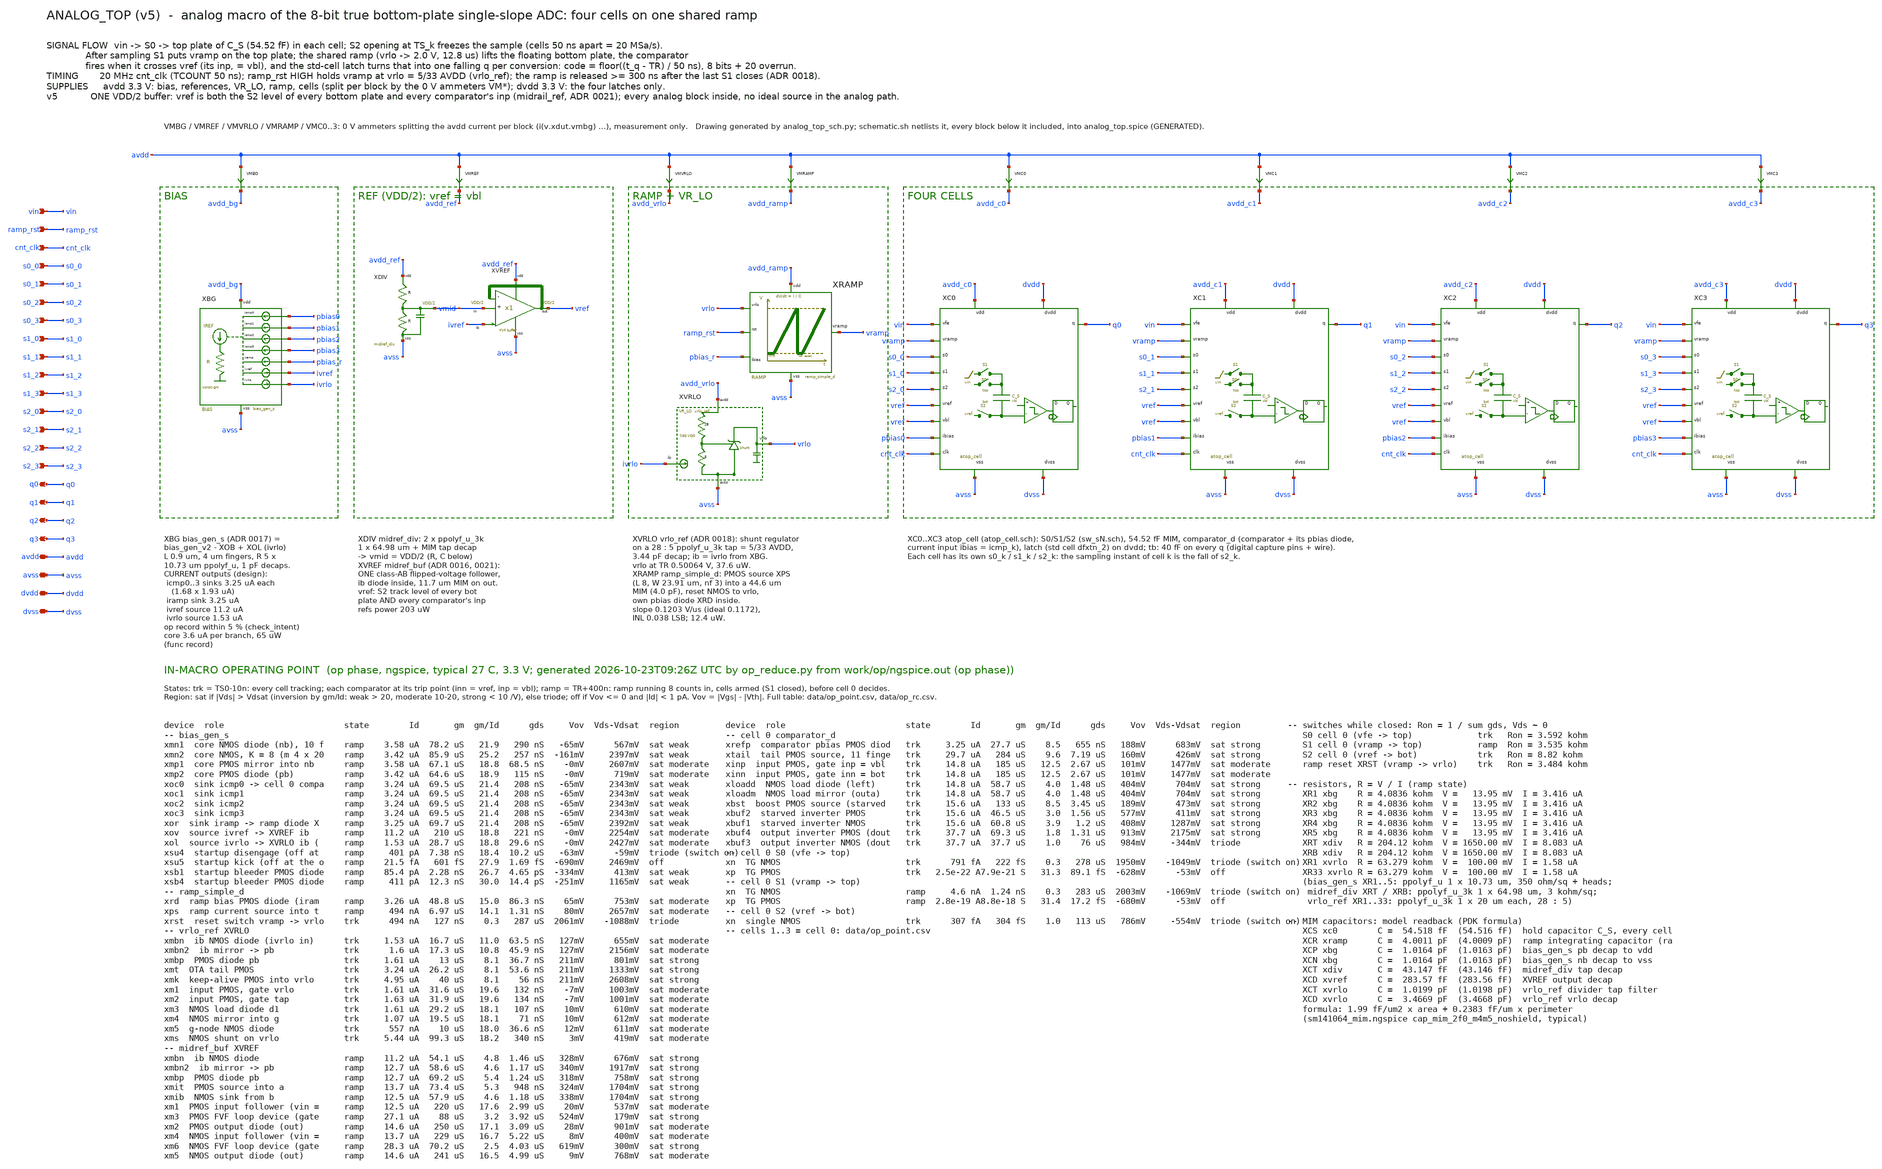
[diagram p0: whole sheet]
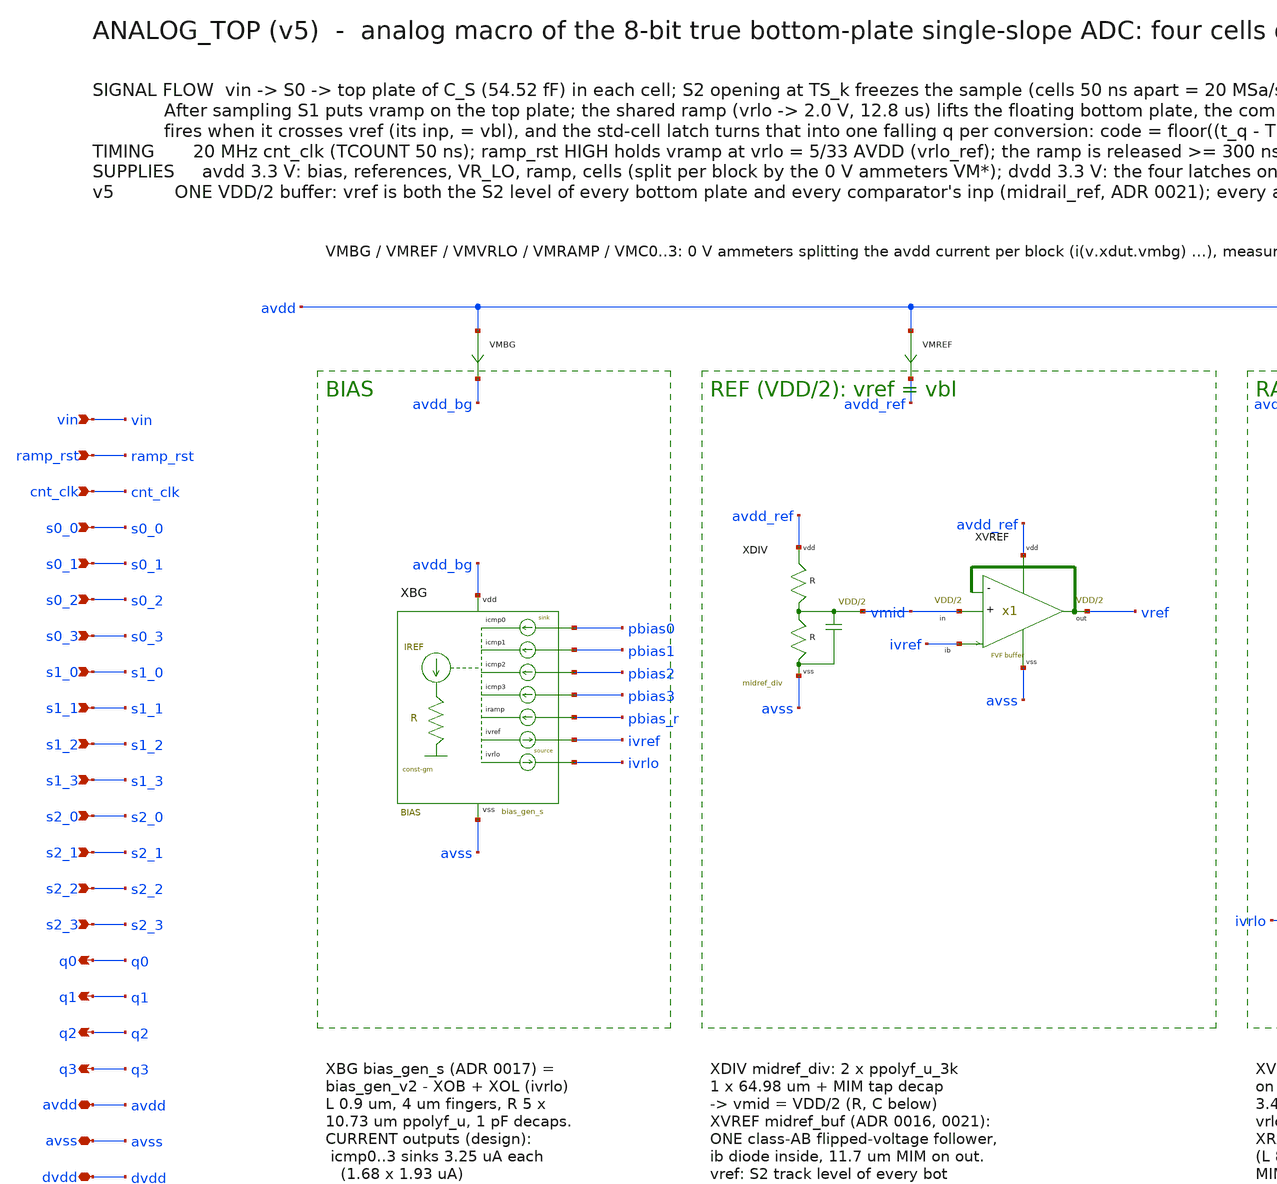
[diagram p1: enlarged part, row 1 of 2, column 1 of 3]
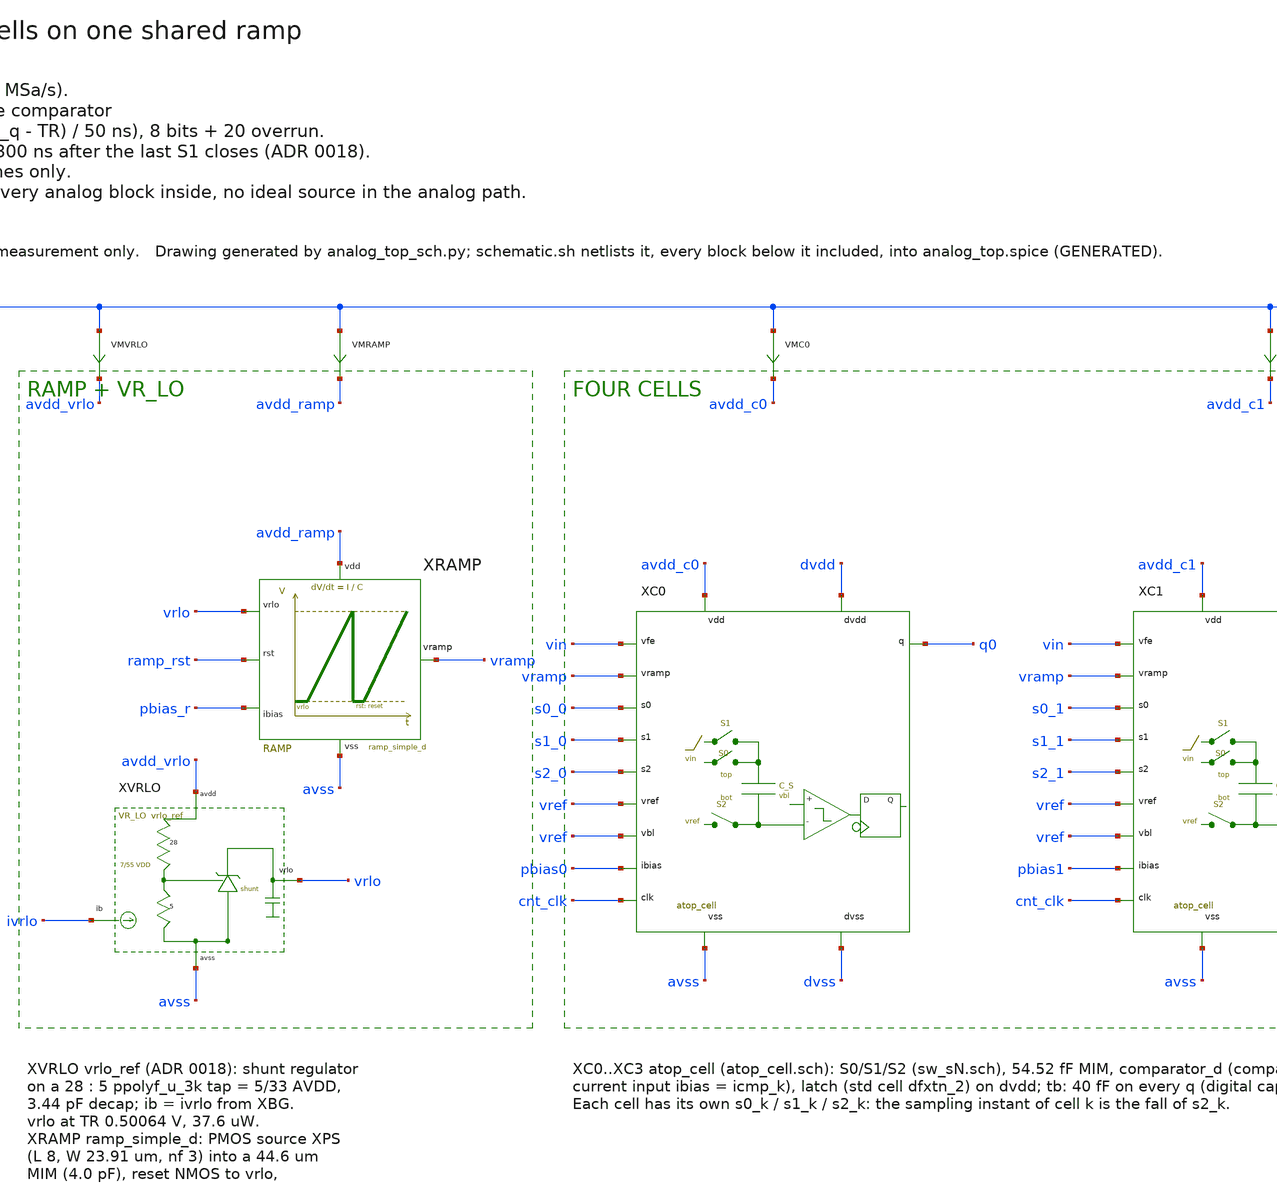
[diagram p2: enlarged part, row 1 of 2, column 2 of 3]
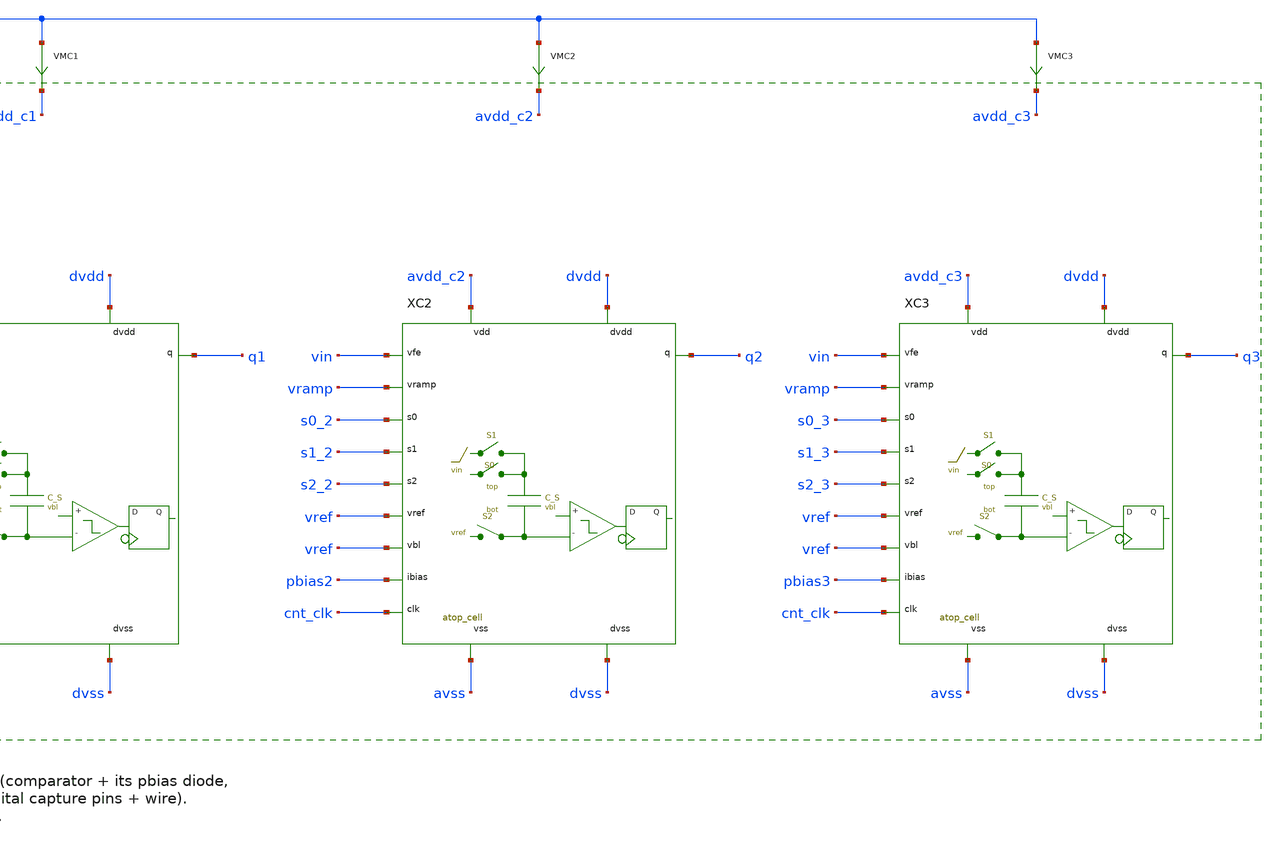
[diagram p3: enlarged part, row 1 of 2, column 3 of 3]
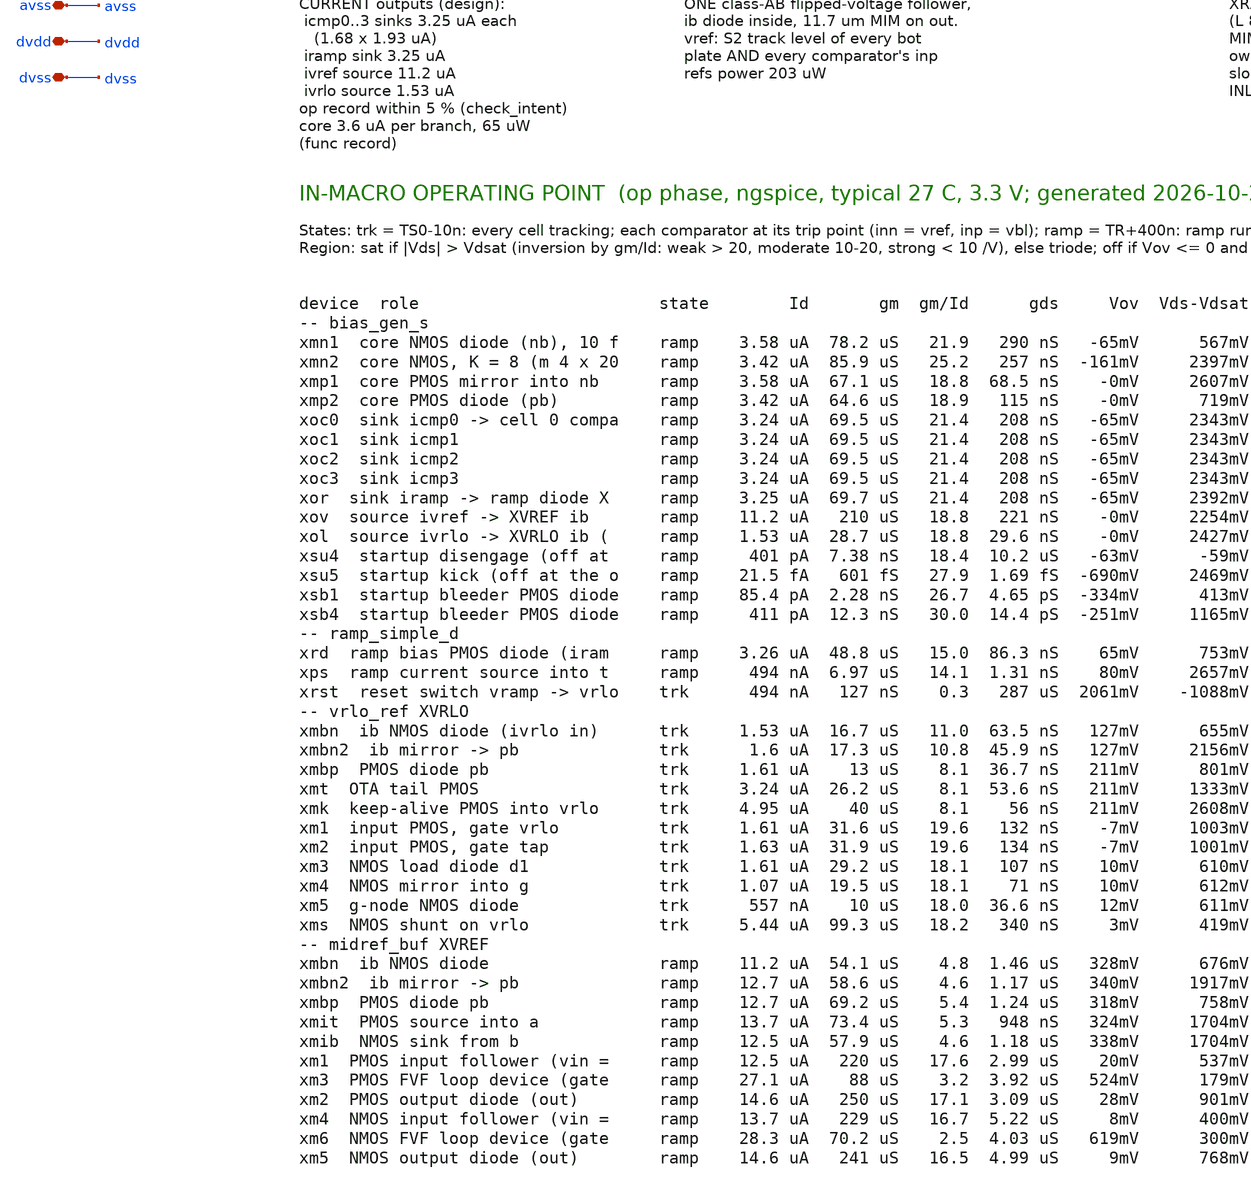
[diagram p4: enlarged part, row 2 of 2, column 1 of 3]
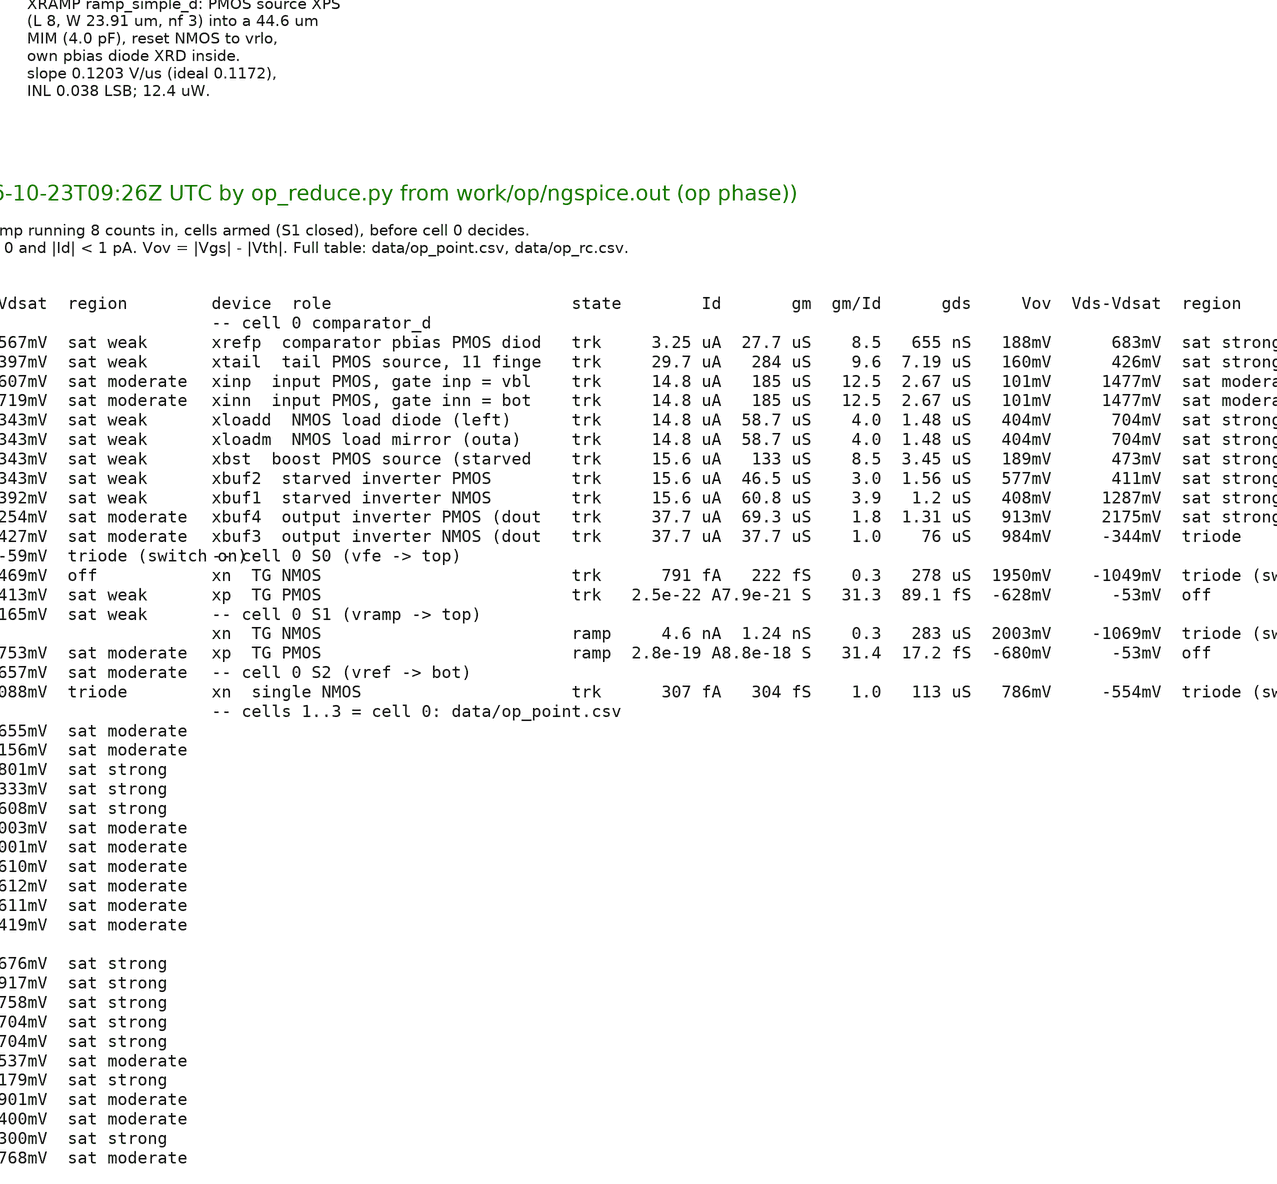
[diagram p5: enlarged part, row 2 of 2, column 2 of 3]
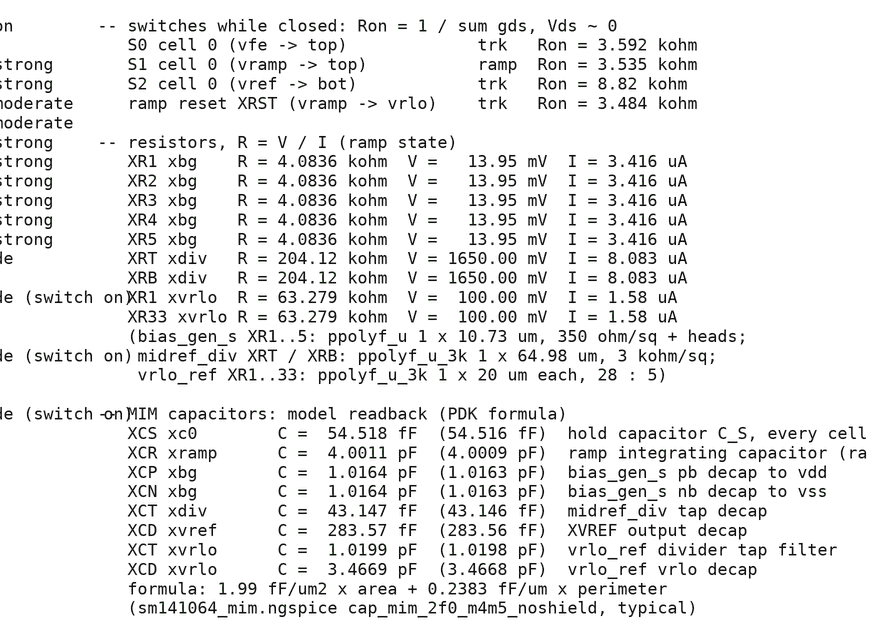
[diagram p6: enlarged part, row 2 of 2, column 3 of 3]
** sch_path: mixed_signal/Analog_top/analog_top.sch
**.subckt analog_top vin ramp_rst cnt_clk s0_0 s0_1 s0_2 s0_3 s1_0 s1_1 s1_2 s1_3 s2_0 s2_1 s2_2
*+ s2_3 q0 q1 q2 q3 avdd avss dvdd dvss
*.ipin vin
*.ipin ramp_rst
*.ipin cnt_clk
*.ipin s0_0
*.ipin s0_1
*.ipin s0_2
*.ipin s0_3
*.ipin s1_0
*.ipin s1_1
*.ipin s1_2
*.ipin s1_3
*.ipin s2_0
*.ipin s2_1
*.ipin s2_2
*.ipin s2_3
*.opin q0
*.opin q1
*.opin q2
*.opin q3
*.iopin avdd
*.iopin avss
*.iopin dvdd
*.iopin dvss
VMBG avdd avdd_bg 0
VMREF avdd avdd_ref 0
VMVRLO avdd avdd_vrlo 0
VMRAMP avdd avdd_ramp 0
VMC0 avdd avdd_c0 0
VMC1 avdd avdd_c1 0
VMC2 avdd avdd_c2 0
VMC3 avdd avdd_c3 0
XBG avdd_bg avss pbias0 pbias1 pbias2 pbias3 pbias_r ivref ivrlo bias_gen_s
XDIV vmid avdd_ref avss midref_div
XVREF vref vmid ivref avdd_ref avss midref_buf
XVRLO vrlo ivrlo avdd_vrlo avss vrlo_ref
XRAMP vramp ramp_rst vrlo pbias_r avdd_ramp avss ramp_simple_d
XC0 vin vramp s0_0 s1_0 s2_0 vref vref pbias0 q0 cnt_clk avdd_c0 avss dvdd dvss atop_cell
XC1 vin vramp s0_1 s1_1 s2_1 vref vref pbias1 q1 cnt_clk avdd_c1 avss dvdd dvss atop_cell
XC2 vin vramp s0_2 s1_2 s2_2 vref vref pbias2 q2 cnt_clk avdd_c2 avss dvdd dvss atop_cell
XC3 vin vramp s0_3 s1_3 s2_3 vref vref pbias3 q3 cnt_clk avdd_c3 avss dvdd dvss atop_cell
**.ends
.end
